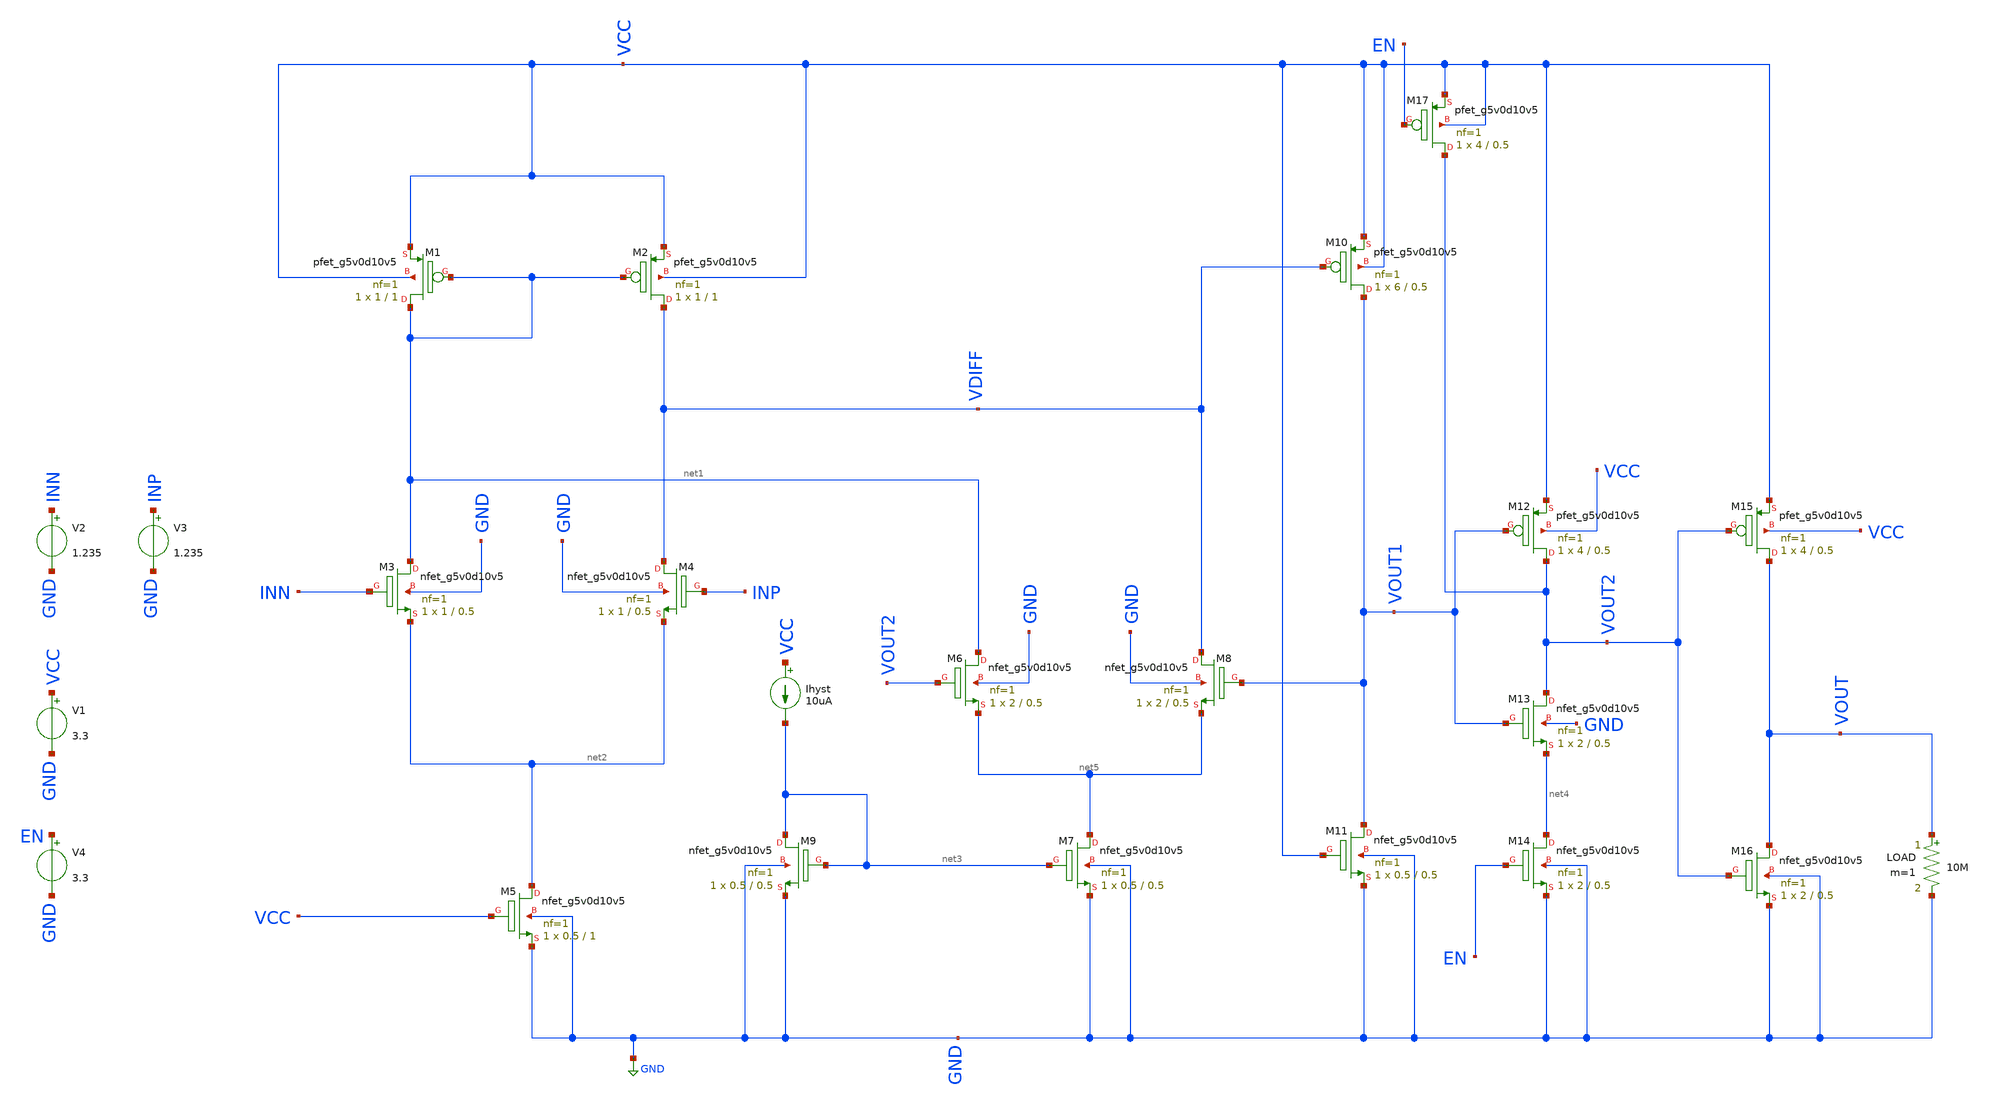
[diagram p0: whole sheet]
** sch_path: Comparator/xschem/Comparator_2.sch
**.subckt Comparator_2
LOAD VOUT GND 10M m=1
Ihyst VCC net3 10uA
V2 INN GND 1.235
V1 VCC GND 3.3
V4 EN GND 3.3
V3 INP GND 1.235
XM1 net1 net1 VCC VCC sky130_fd_pr__pfet_g5v0d10v5 L=1 W=1 nf=1 ad='int((nf+1)/2) * W/nf * 0.29' as='int((nf+2)/2) * W/nf * 0.29'
+ pd='2*int((nf+1)/2) * (W/nf + 0.29)' ps='2*int((nf+2)/2) * (W/nf + 0.29)' nrd='0.29 / W' nrs='0.29 / W'
+ sa=0 sb=0 sd=0 mult=1 m=1
XM2 VDIFF net1 VCC VCC sky130_fd_pr__pfet_g5v0d10v5 L=1 W=1 nf=1 ad='int((nf+1)/2) * W/nf * 0.29' as='int((nf+2)/2) * W/nf * 0.29'
+ pd='2*int((nf+1)/2) * (W/nf + 0.29)' ps='2*int((nf+2)/2) * (W/nf + 0.29)' nrd='0.29 / W' nrs='0.29 / W'
+ sa=0 sb=0 sd=0 mult=1 m=1
XM3 net1 INN net2 GND sky130_fd_pr__nfet_g5v0d10v5 L=0.5 W=1 nf=1 ad='int((nf+1)/2) * W/nf * 0.29' as='int((nf+2)/2) * W/nf * 0.29'
+ pd='2*int((nf+1)/2) * (W/nf + 0.29)' ps='2*int((nf+2)/2) * (W/nf + 0.29)' nrd='0.29 / W' nrs='0.29 / W'
+ sa=0 sb=0 sd=0 mult=1 m=1
XM4 VDIFF INP net2 GND sky130_fd_pr__nfet_g5v0d10v5 L=0.5 W=1 nf=1 ad='int((nf+1)/2) * W/nf * 0.29' as='int((nf+2)/2) * W/nf * 0.29'
+ pd='2*int((nf+1)/2) * (W/nf + 0.29)' ps='2*int((nf+2)/2) * (W/nf + 0.29)' nrd='0.29 / W' nrs='0.29 / W'
+ sa=0 sb=0 sd=0 mult=1 m=1
XM5 net2 VCC GND GND sky130_fd_pr__nfet_g5v0d10v5 L=1 W=0.5 nf=1 ad='int((nf+1)/2) * W/nf * 0.29' as='int((nf+2)/2) * W/nf * 0.29'
+ pd='2*int((nf+1)/2) * (W/nf + 0.29)' ps='2*int((nf+2)/2) * (W/nf + 0.29)' nrd='0.29 / W' nrs='0.29 / W'
+ sa=0 sb=0 sd=0 mult=1 m=1
XM6 net1 VOUT2 net5 GND sky130_fd_pr__nfet_g5v0d10v5 L=0.5 W=2 nf=1 ad='int((nf+1)/2) * W/nf * 0.29'
+ as='int((nf+2)/2) * W/nf * 0.29' pd='2*int((nf+1)/2) * (W/nf + 0.29)' ps='2*int((nf+2)/2) * (W/nf + 0.29)'
+ nrd='0.29 / W' nrs='0.29 / W' sa=0 sb=0 sd=0 mult=1 m=1
XM7 net5 net3 GND GND sky130_fd_pr__nfet_g5v0d10v5 L=0.5 W=0.5 nf=1 ad='int((nf+1)/2) * W/nf * 0.29'
+ as='int((nf+2)/2) * W/nf * 0.29' pd='2*int((nf+1)/2) * (W/nf + 0.29)' ps='2*int((nf+2)/2) * (W/nf + 0.29)'
+ nrd='0.29 / W' nrs='0.29 / W' sa=0 sb=0 sd=0 mult=1 m=1
XM8 VDIFF VOUT1 net5 GND sky130_fd_pr__nfet_g5v0d10v5 L=0.5 W=2 nf=1 ad='int((nf+1)/2) * W/nf * 0.29'
+ as='int((nf+2)/2) * W/nf * 0.29' pd='2*int((nf+1)/2) * (W/nf + 0.29)' ps='2*int((nf+2)/2) * (W/nf + 0.29)'
+ nrd='0.29 / W' nrs='0.29 / W' sa=0 sb=0 sd=0 mult=1 m=1
XM14 net4 EN GND GND sky130_fd_pr__nfet_g5v0d10v5 L=0.5 W=2 nf=1 ad='int((nf+1)/2) * W/nf * 0.29' as='int((nf+2)/2) * W/nf * 0.29'
+ pd='2*int((nf+1)/2) * (W/nf + 0.29)' ps='2*int((nf+2)/2) * (W/nf + 0.29)' nrd='0.29 / W' nrs='0.29 / W'
+ sa=0 sb=0 sd=0 mult=1 m=1
XM11 VOUT1 VCC GND GND sky130_fd_pr__nfet_g5v0d10v5 L=0.5 W=0.5 nf=1 ad='int((nf+1)/2) * W/nf * 0.29'
+ as='int((nf+2)/2) * W/nf * 0.29' pd='2*int((nf+1)/2) * (W/nf + 0.29)' ps='2*int((nf+2)/2) * (W/nf + 0.29)'
+ nrd='0.29 / W' nrs='0.29 / W' sa=0 sb=0 sd=0 mult=1 m=1
XM12 VOUT2 VOUT1 VCC VCC sky130_fd_pr__pfet_g5v0d10v5 L=0.5 W=4 nf=1 ad='int((nf+1)/2) * W/nf * 0.29'
+ as='int((nf+2)/2) * W/nf * 0.29' pd='2*int((nf+1)/2) * (W/nf + 0.29)' ps='2*int((nf+2)/2) * (W/nf + 0.29)'
+ nrd='0.29 / W' nrs='0.29 / W' sa=0 sb=0 sd=0 mult=1 m=1
XM13 VOUT2 VOUT1 net4 GND sky130_fd_pr__nfet_g5v0d10v5 L=0.5 W=2 nf=1 ad='int((nf+1)/2) * W/nf * 0.29'
+ as='int((nf+2)/2) * W/nf * 0.29' pd='2*int((nf+1)/2) * (W/nf + 0.29)' ps='2*int((nf+2)/2) * (W/nf + 0.29)'
+ nrd='0.29 / W' nrs='0.29 / W' sa=0 sb=0 sd=0 mult=1 m=1
XM16 VOUT VOUT2 GND GND sky130_fd_pr__nfet_g5v0d10v5 L=0.5 W=2 nf=1 ad='int((nf+1)/2) * W/nf * 0.29'
+ as='int((nf+2)/2) * W/nf * 0.29' pd='2*int((nf+1)/2) * (W/nf + 0.29)' ps='2*int((nf+2)/2) * (W/nf + 0.29)'
+ nrd='0.29 / W' nrs='0.29 / W' sa=0 sb=0 sd=0 mult=1 m=1
XM15 VOUT VOUT2 VCC VCC sky130_fd_pr__pfet_g5v0d10v5 L=0.5 W=4 nf=1 ad='int((nf+1)/2) * W/nf * 0.29'
+ as='int((nf+2)/2) * W/nf * 0.29' pd='2*int((nf+1)/2) * (W/nf + 0.29)' ps='2*int((nf+2)/2) * (W/nf + 0.29)'
+ nrd='0.29 / W' nrs='0.29 / W' sa=0 sb=0 sd=0 mult=1 m=1
XM17 VOUT2 EN VCC VCC sky130_fd_pr__pfet_g5v0d10v5 L=0.5 W=4 nf=1 ad='int((nf+1)/2) * W/nf * 0.29' as='int((nf+2)/2) * W/nf * 0.29'
+ pd='2*int((nf+1)/2) * (W/nf + 0.29)' ps='2*int((nf+2)/2) * (W/nf + 0.29)' nrd='0.29 / W' nrs='0.29 / W'
+ sa=0 sb=0 sd=0 mult=1 m=1
XM10 VOUT1 VDIFF VCC VCC sky130_fd_pr__pfet_g5v0d10v5 L=0.5 W=6 nf=1 ad='int((nf+1)/2) * W/nf * 0.29'
+ as='int((nf+2)/2) * W/nf * 0.29' pd='2*int((nf+1)/2) * (W/nf + 0.29)' ps='2*int((nf+2)/2) * (W/nf + 0.29)'
+ nrd='0.29 / W' nrs='0.29 / W' sa=0 sb=0 sd=0 mult=1 m=1
XM9 net3 net3 GND GND sky130_fd_pr__nfet_g5v0d10v5 L=0.5 W=0.5 nf=1 ad='int((nf+1)/2) * W/nf * 0.29'
+ as='int((nf+2)/2) * W/nf * 0.29' pd='2*int((nf+1)/2) * (W/nf + 0.29)' ps='2*int((nf+2)/2) * (W/nf + 0.29)'
+ nrd='0.29 / W' nrs='0.29 / W' sa=0 sb=0 sd=0 mult=1 m=1
**.ends
.GLOBAL GND
.end
